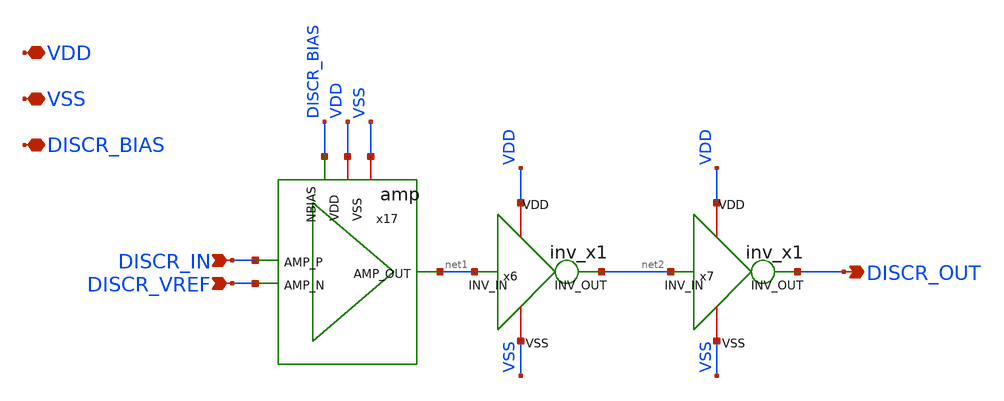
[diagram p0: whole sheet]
** sch_path: xschem/ndiscr.sch
**.subckt ndiscr VDD VSS DISCR_IN DISCR_VREF DISCR_OUT DISCR_BIAS
*.iopin VDD
*.iopin VSS
*.ipin DISCR_IN
*.ipin DISCR_VREF
*.opin DISCR_OUT
*.iopin DISCR_BIAS
x6 VDD VSS net2 net1 inv_x1
x7 VDD VSS DISCR_OUT net2 inv_x1
x17 VDD VSS net1 DISCR_IN DISCR_VREF DISCR_BIAS amp
**.ends

* expanding   symbol:  inv_x1.sym # of pins=4
** sym_path: xschem/inv_x1.sym
** sch_path: xschem/inv_x1.sch
.subckt inv_x1 VDD VSS INV_OUT INV_IN
*.ipin INV_IN
*.opin INV_OUT
*.iopin VDD
*.iopin VSS
XM3 INV_OUT INV_IN VDD VDD sky130_fd_pr__pfet_01v8 L=0.15 W=1 nf=1 ad='int((nf+1)/2) * W/nf * 0.29' as='int((nf+2)/2) * W/nf * 0.29'
+ pd='2*int((nf+1)/2) * (W/nf + 0.29)' ps='2*int((nf+2)/2) * (W/nf + 0.29)' nrd='0.29 / W' nrs='0.29 / W'
+ sa=0 sb=0 sd=0 mult=1 m=1
XM5 INV_OUT INV_IN VSS VSS sky130_fd_pr__nfet_01v8 L=0.15 W=1 nf=1 ad='int((nf+1)/2) * W/nf * 0.29' as='int((nf+2)/2) * W/nf * 0.29'
+ pd='2*int((nf+1)/2) * (W/nf + 0.29)' ps='2*int((nf+2)/2) * (W/nf + 0.29)' nrd='0.29 / W' nrs='0.29 / W'
+ sa=0 sb=0 sd=0 mult=1 m=1
.ends


* expanding   symbol:  amp.sym # of pins=6
** sym_path: xschem/amp.sym
** sch_path: xschem/amp.sch
.subckt amp VDD VSS AMP_OUT AMP_P AMP_N NBIAS
*.ipin AMP_P
*.ipin AMP_N
*.opin AMP_OUT
*.ipin NBIAS
*.iopin VDD
*.iopin VSS
XM3 VFOLD VFOLD VDD VDD sky130_fd_pr__pfet_01v8 L=0.15 W=10 nf=1 ad='int((nf+1)/2) * W/nf * 0.29' as='int((nf+2)/2) * W/nf * 0.29'
+ pd='2*int((nf+1)/2) * (W/nf + 0.29)' ps='2*int((nf+2)/2) * (W/nf + 0.29)' nrd='0.29 / W' nrs='0.29 / W'
+ sa=0 sb=0 sd=0 mult=1 m=1
XM4 AMP_OUT AMP_N VTAIL VSS sky130_fd_pr__nfet_01v8 L=0.15 W=10 nf=1 ad='int((nf+1)/2) * W/nf * 0.29'
+ as='int((nf+2)/2) * W/nf * 0.29' pd='2*int((nf+1)/2) * (W/nf + 0.29)' ps='2*int((nf+2)/2) * (W/nf + 0.29)'
+ nrd='0.29 / W' nrs='0.29 / W' sa=0 sb=0 sd=0 mult=1 m=1
XM1 AMP_OUT VFOLD VDD VDD sky130_fd_pr__pfet_01v8 L=0.15 W=10 nf=1 ad='int((nf+1)/2) * W/nf * 0.29' as='int((nf+2)/2) * W/nf * 0.29'
+ pd='2*int((nf+1)/2) * (W/nf + 0.29)' ps='2*int((nf+2)/2) * (W/nf + 0.29)' nrd='0.29 / W' nrs='0.29 / W'
+ sa=0 sb=0 sd=0 mult=1 m=1
XM5 VFOLD AMP_P VTAIL VSS sky130_fd_pr__nfet_01v8 L=0.15 W=10 nf=1 ad='int((nf+1)/2) * W/nf * 0.29' as='int((nf+2)/2) * W/nf * 0.29'
+ pd='2*int((nf+1)/2) * (W/nf + 0.29)' ps='2*int((nf+2)/2) * (W/nf + 0.29)' nrd='0.29 / W' nrs='0.29 / W'
+ sa=0 sb=0 sd=0 mult=1 m=1
XM2 VTAIL NBIAS VSS VSS sky130_fd_pr__nfet_01v8 L=1 W=1 nf=1 ad='int((nf+1)/2) * W/nf * 0.29' as='int((nf+2)/2) * W/nf * 0.29'
+ pd='2*int((nf+1)/2) * (W/nf + 0.29)' ps='2*int((nf+2)/2) * (W/nf + 0.29)' nrd='0.29 / W' nrs='0.29 / W'
+ sa=0 sb=0 sd=0 mult=4 m=4
.ends

.end
